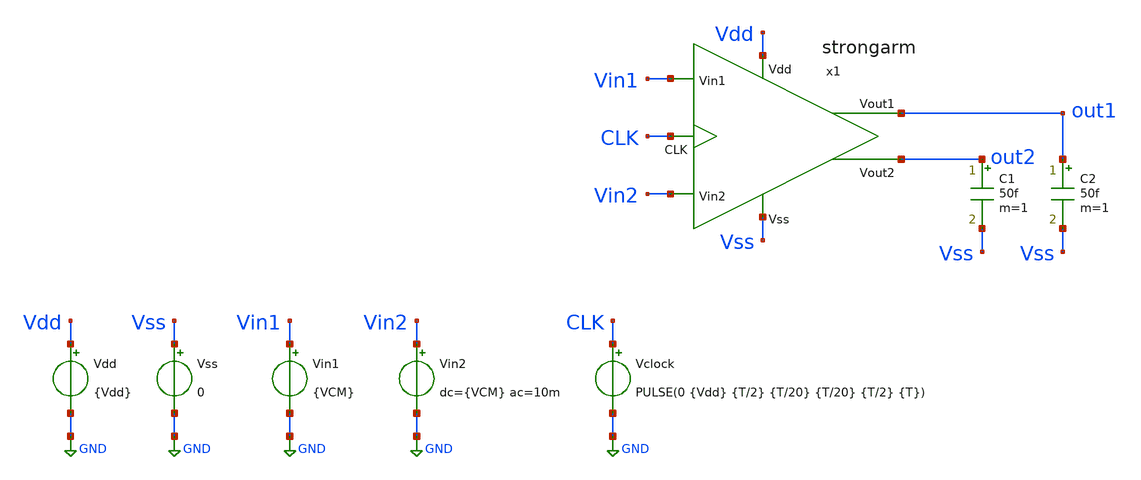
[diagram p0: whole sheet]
** sch_path: xschem/TB/TB_Tran_SA.sch
**.subckt TB_Tran_SA
Vdd Vdd GND {Vdd}
x1 out2 out1 Vdd Vss Vin2 Vin1 CLK strongarm
Vss Vss GND 0
C1 out2 Vss 50f m=1
C2 out1 Vss 50f m=1
Vin1 Vin1 GND {VCM}
Vin2 Vin2 GND dc={VCM} ac=10m
Vclock CLK GND PULSE(0 {Vdd} {T/2} {T/20} {T/20} {T/2} {T})
**** begin user architecture code


.param Vdd = 1.2
.param VCM = 0.6





.lib cornerMOSlv.lib mos_tt




** TRANSISTORES NMOS

.param W12 = 0.6u
.param L12 = 0.13u
.param M12 = 1

.param W34 = 0.3u
.param L34 = 0.13u
.param M34 = 1

.param W56 = 0.3u
.param L56 = 0.13u
.param M56 = 1

.param W7  = 0.3u
.param L7  = 0.13u
.param M7  = 1

.param W89 = 0.3u
.param L89 = 0.13u
.param M89 = 1

.param Wab = 0.3u
.param Lab = 0.13u
.param Mab = 1




.control
.param T = 30n
*.param SimTime = 3*T + 100n
save all  @n.x1.xm1.nsg13_lv_nmos[gm]  @n.x1.xm2.nsg13_lv_nmos[gm]  @n.x1.xm1.nsg13_lv_nmos[ids]
+  @n.x1.xm2.nsg13_lv_nmos[ids]
tran 10p 40n
let gm1 = @n.x1.xm1.nsg13_lv_nmos[gm]
let ids1= @n.x1.xm1.nsg13_lv_nmos[ids]

meas tran Amp_t TRIG AT=15n TARG v(out1) VAL=0.6 CROSS=1
meas tran reg_t TRIG v(out1) VAL=0.6 CROSS=1 TARG v(out1) VAL=0.01 CROSS=1
plot v(out1) v(out2)
plot v(x1.Q) (v(CLK)/2 +0.2)
plot v(x1.P)
.endc


**** end user architecture code
**.ends

* expanding   symbol:  ../sch/strongarm.sym # of pins=7
** sym_path: xschem/sch/strongarm.sym
** sch_path: xschem/sch/strongarm.sch
.subckt strongarm Vout2 Vout1 Vdd Vss Vin2 Vin1 CLK
*.opin Vout2
*.opin Vout1
*.ipin Vin1
*.ipin Vin2
*.ipin CLK
*.ipin Vss
*.ipin Vdd
XM1 common Vin1 P Vss sg13_lv_nmos w={W12} l={L12} ng={F12} m={M12} mm_ok=1
XM2 common Vin2 Q Vss sg13_lv_nmos w={W12} l={L12} ng={F12} m={M12} mm_ok=1
XM3 P Vout2 Vout1 Vss sg13_lv_nmos w={W34} l={L34} ng={F34} m={M34} mm_ok=1
XM4 Q Vout1 Vout2 Vss sg13_lv_nmos w={W34} l={L34} ng={F34} m={M34} mm_ok=1
XM6 Vout2 Vout1 Vdd Vdd sg13_lv_pmos w={W56} l={L56} ng={F56} m={M56} mm_ok=1
XM5 Vout1 Vout2 Vdd Vdd sg13_lv_pmos w={W56} l={L56} ng={F56} m={M56} mm_ok=1
XM7 Vss CLK common Vss sg13_lv_nmos w={W7} l={L7} ng={F7} m={M7} mm_ok=1
XM8 P CLK Vdd Vdd sg13_lv_pmos w={W89} l={L89} ng={F89} m={M89} mm_ok=1
XM9 Q CLK Vdd Vdd sg13_lv_pmos w={W89} l={L89} ng={F89} m={M89} mm_ok=1
XM11 Vdd CLK Vout2 Vdd sg13_lv_pmos w={Wab} l={Lab} ng={Fab} m={Mab} mm_ok=1
XM10 Vdd CLK Vout1 Vdd sg13_lv_pmos w={Wab} l={Lab} ng={Fab} m={Mab} mm_ok=1
.ends

.GLOBAL GND
.end
